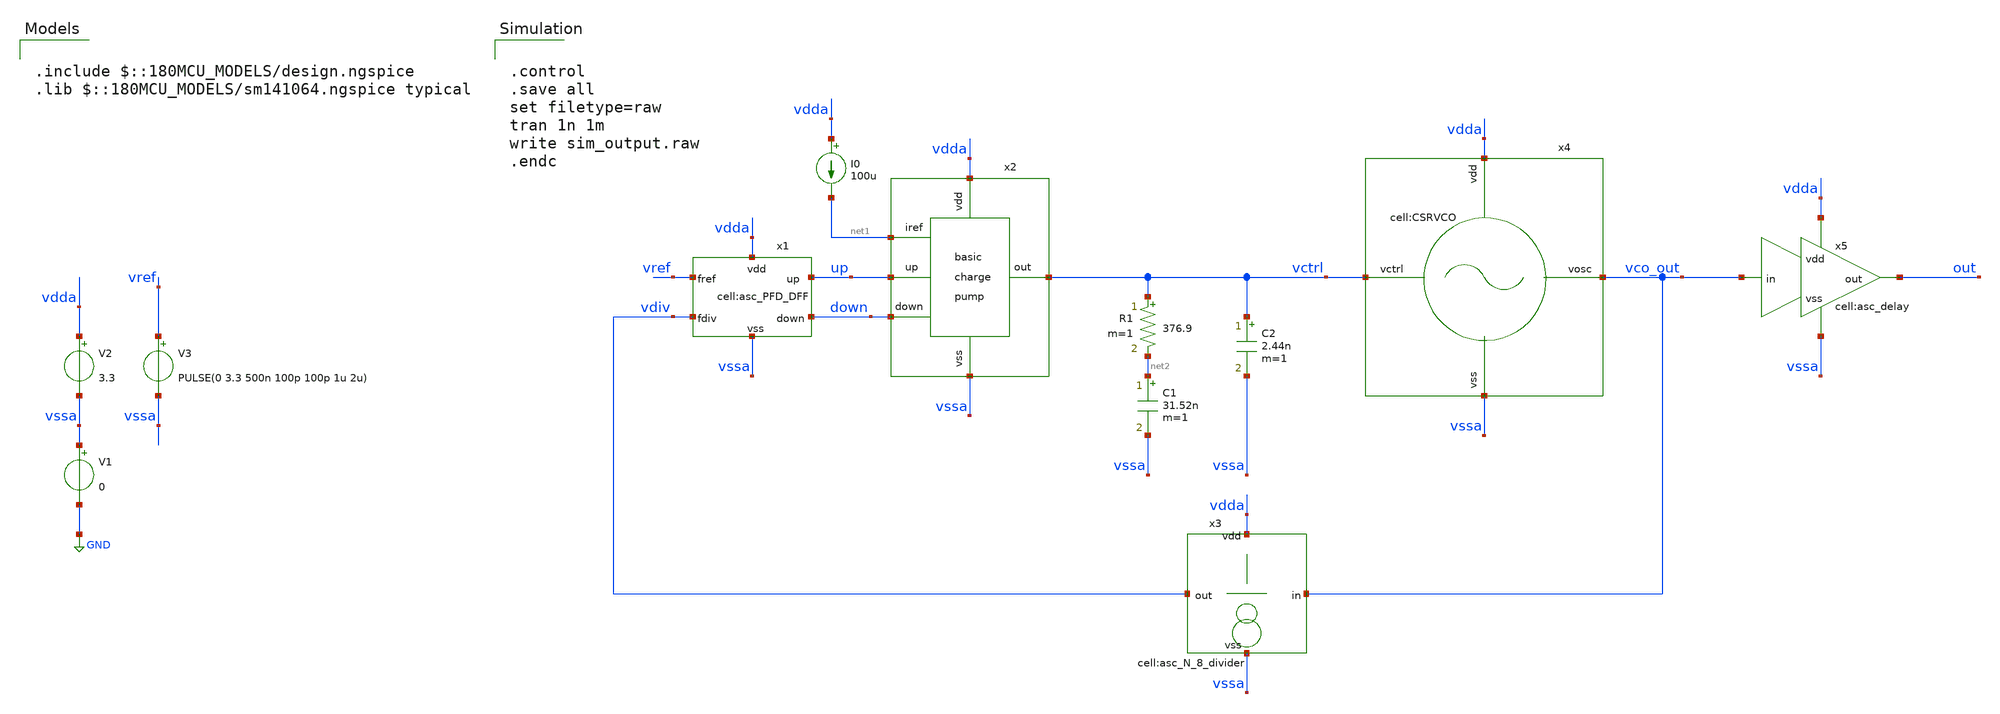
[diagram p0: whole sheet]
** sch_path: designs/libs/tb_analog/tb_poc_pll/tb_poc_pll.sch
**.subckt tb_poc_pll
V1 vssa GND 0
V2 vdda vssa 3.3
V3 vref vssa PULSE(0 3.3 500n 100p 100p 1u 2u)
x1 vdda vssa down up vref vdiv asc_PFD_DFF
x2 vdda vctrl vssa down up net1 asc_basic_pump
I0 vdda net1 100u
x3 vco_out vdiv vdda vssa asc_N_8_divider
x4 vctrl vdda vssa vco_out CSRVCO
x5 vco_out vssa out vdda asc_delay
C1 net2 vssa 31.52n m=1
C2 vctrl vssa 2.44n m=1
R1 vctrl net2 376.9 m=1
**** begin user architecture code

.include $::180MCU_MODELS/design.ngspice
.lib $::180MCU_MODELS/sm141064.ngspice typical



.control
.save all
set filetype=raw
tran 1n 1m
write sim_output.raw
.endc


**** end user architecture code
**.ends
.GLOBAL GND
.end
